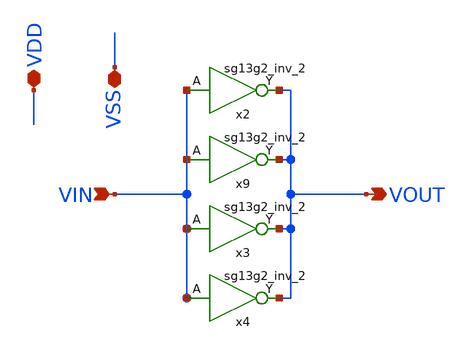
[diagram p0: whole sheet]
** sch_path: QDLL6501-main/schematic/xschem/INV4.sch
* IHP-GmbH/IHP-Open-PDK/ihp-sg13g2/libs.tech/xschem/sg13g2_stdcells/sg13g2_inv_2.sch:
* Copyright 2023 IHP PDK Authors
* Licensed under the Apache License, Version 2.0 (the "License");
**.subckt INV4 VIN VDD VSS VOUT
*.ipin VIN
*.iopin VDD
*.iopin VSS
*.opin VOUT
x9 VOUT VIN VDD VSS sg13g2_inv_2
x2 VOUT VIN VDD VSS sg13g2_inv_2
x3 VOUT VIN VDD VSS sg13g2_inv_2
x4 VOUT VIN VDD VSS sg13g2_inv_2
**.ends

* expanding   symbol:  sg13g2_stdcells/sg13g2_inv_2.sym # of pins=2
** sym_path: sg13g2_stdcells/sg13g2_inv_2.sym
** sch_path: sg13g2_stdcells/sg13g2_inv_2.sch
.subckt sg13g2_inv_2 Y A VDD VSS
*.opin Y
*.ipin A
*.iopin VDD
*.iopin VSS
XM1 Y A VSS VSS sg13_lv_nmos w=1.48u l=130.00n ng=2 m=1 mm_ok=1
XM2 Y A VDD VDD sg13_lv_pmos w=2.24u l=130.00n ng=2 m=1 mm_ok=1
.ends

.end
